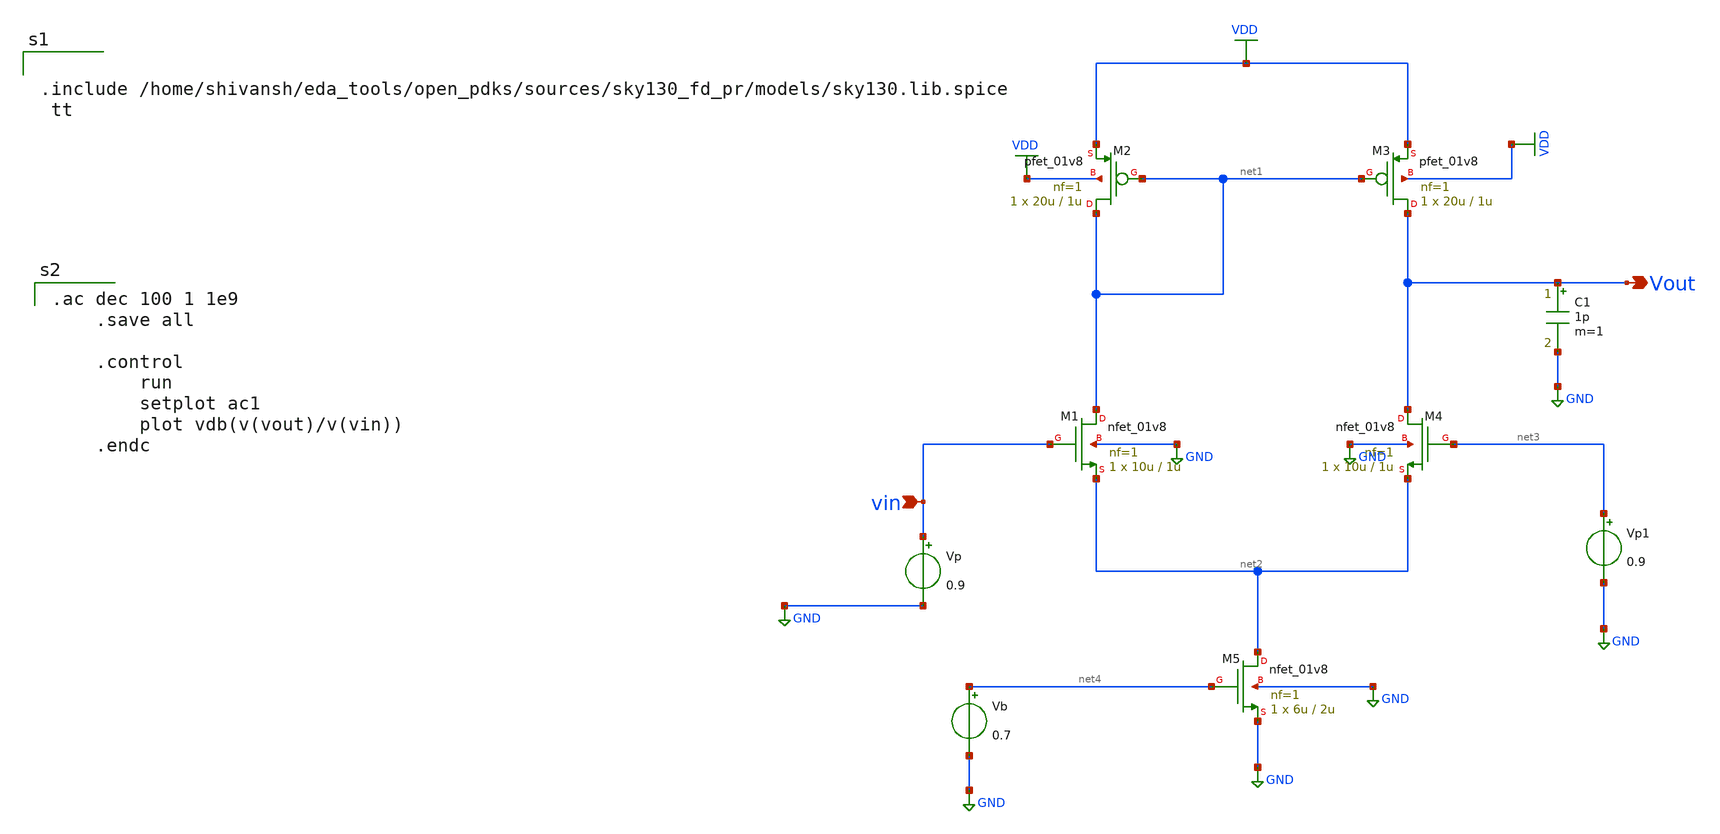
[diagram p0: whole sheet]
** sch_path: 5t.sch
**.subckt 5t Vout vin
*.opin Vout
*.ipin vin
XM1 net1 vin net2 GND sky130_fd_pr__nfet_01v8 L=1u W=10u nf=1 ad='int((1 + 1)/2) * 10u / 1 * 0.29' as='int((1 + 2)/2) * 10u / 1 * 0.29'
+ pd='2*int((1 + 1)/2) * (10u / 1 + 0.29)' ps='2*int((1 + 2)/2) * (10u / 1 + 0.29)' nrd='0.29 / 10u ' nrs='0.29 / 10u '
+ sa=0 sb=0 sd=0 mult=1 m=1
XM2 net1 net1 VDD VDD sky130_fd_pr__pfet_01v8 L=1u W=20u nf=1 ad='int((1 + 1)/2) * 20u / 1 * 0.29' as='int((1 + 2)/2) * 20u / 1 * 0.29'
+ pd='2*int((1 + 1)/2) * (20u / 1 + 0.29)' ps='2*int((1 + 2)/2) * (20u / 1 + 0.29)' nrd='0.29 / 20u ' nrs='0.29 / 20u '
+ sa=0 sb=0 sd=0 mult=1 m=1
XM3 Vout net1 VDD VDD sky130_fd_pr__pfet_01v8 L=1u W=20u nf=1 ad='int((1 + 1)/2) * 20u / 1 * 0.29' as='int((1 + 2)/2) * 20u / 1 * 0.29'
+ pd='2*int((1 + 1)/2) * (20u / 1 + 0.29)' ps='2*int((1 + 2)/2) * (20u / 1 + 0.29)' nrd='0.29 / 20u ' nrs='0.29 / 20u '
+ sa=0 sb=0 sd=0 mult=1 m=1
XM4 Vout net3 net2 GND sky130_fd_pr__nfet_01v8 L=1u W=10u nf=1 ad='int((1 + 1)/2) * 10u / 1 * 0.29' as='int((1 + 2)/2) * 10u / 1 * 0.29'
+ pd='2*int((1 + 1)/2) * (10u / 1 + 0.29)' ps='2*int((1 + 2)/2) * (10u / 1 + 0.29)' nrd='0.29 / 10u ' nrs='0.29 / 10u '
+ sa=0 sb=0 sd=0 mult=1 m=1
XM5 net2 net4 GND GND sky130_fd_pr__nfet_01v8 L=2u W=6u nf=1 ad='int((1 + 1)/2) * 6u / 1 * 0.29' as='int((1 + 2)/2) * 6u / 1 * 0.29'
+ pd='2*int((1 + 1)/2) * (6u / 1 + 0.29)' ps='2*int((1 + 2)/2) * (6u / 1 + 0.29)' nrd='0.29 / 6u ' nrs='0.29 / 6u '
+ sa=0 sb=0 sd=0 mult=1 m=1
C1 Vout GND 1p m=1
Vp1 net3 GND 0.9
Vb net4 GND 0.7
Vp vin GND 0.9
**** begin user architecture code


.include /home/shivansh/eda_tools/open_pdks/sources/sky130_fd_pr/models/sky130.lib.spice
 tt




.ac dec 100 1 1e9
    .save all

    .control
        run
        setplot ac1
        plot vdb(v(vout)/v(vin))
    .endc

**** end user architecture code
**.ends
.GLOBAL VDD
.GLOBAL GND
.end
